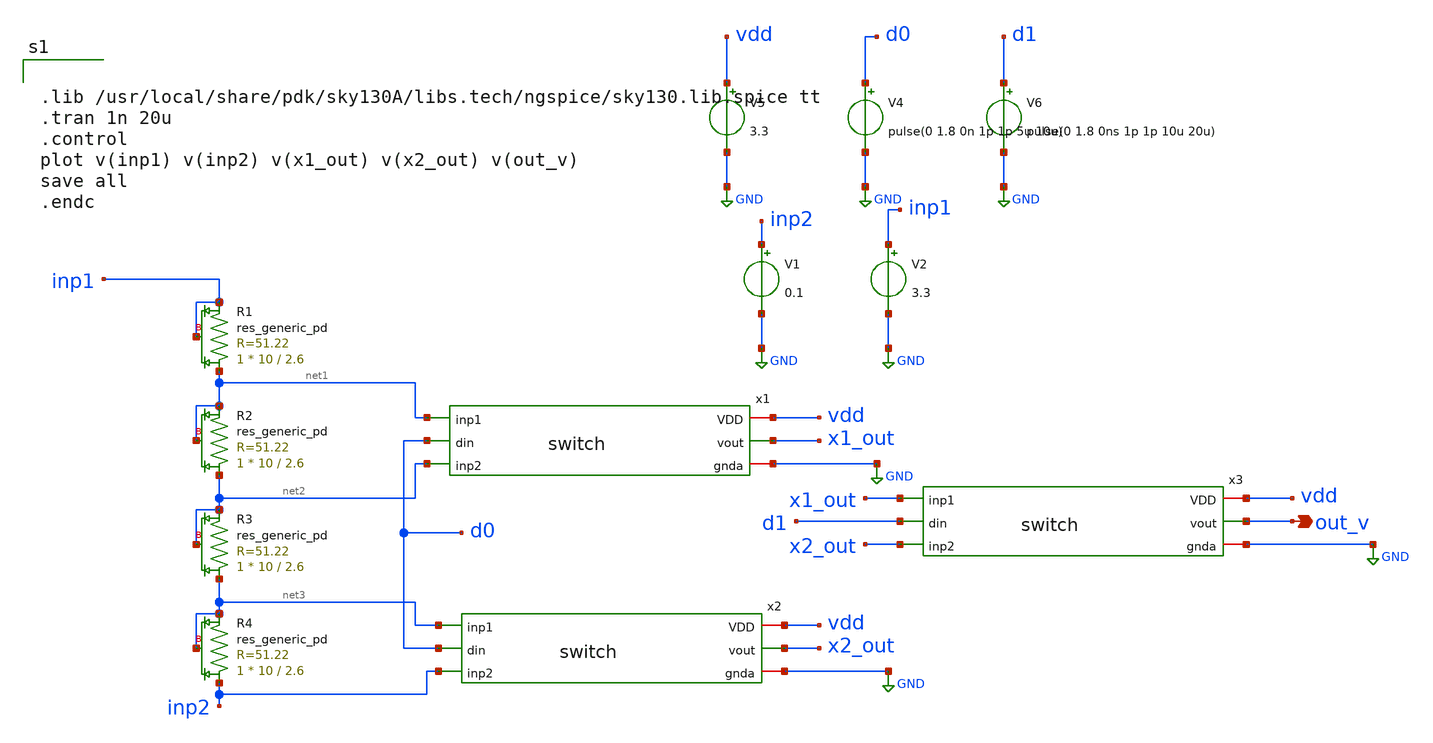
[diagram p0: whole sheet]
** sch_path: week7/pre-layout/two_bit_DAC_tb.sch
**.subckt two_bit_DAC_tb out_v
*.opin out_v
XR1 net1 inp1 inp1 sky130_fd_pr__res_generic_pd W=10 L=2.6 mult=1 m=1
XR2 net2 net1 net1 sky130_fd_pr__res_generic_pd W=10 L=2.6 mult=1 m=1
XR3 net3 net2 net2 sky130_fd_pr__res_generic_pd W=10 L=2.6 mult=1 m=1
XR4 inp2 net3 net3 sky130_fd_pr__res_generic_pd W=10 L=2.6 mult=1 m=1
V1 inp2 GND 0.1
V2 inp1 GND 3.3
V4 d0 GND pulse(0 1.8 0n 1p 1p 5u 10u)
V5 vdd GND 3.3
V6 d1 GND pulse(0 1.8 0ns 1p 1p 10u 20u)
x1 net1 vdd d0 x1_out GND net2 switch
x2 net3 vdd d0 x2_out GND inp2 switch
x3 x1_out vdd d1 out_v GND x2_out switch
**** begin user architecture code


.lib /usr/local/share/pdk/sky130A/libs.tech/ngspice/sky130.lib.spice tt
.tran 1n 20u
.control
plot v(inp1) v(inp2) v(x1_out) v(x2_out) v(out_v)
save all
.endc


**** end user architecture code
**.ends

* expanding   symbol:  switch.sym # of pins=6
** sym_path: week7/pre-layout/switch.sym
** sch_path: week7/pre-layout/switch.sch
.subckt switch inp1 VDD din vout gnda inp2
*.ipin din
*.iopin VDD
*.ipin inp1
*.ipin inp2
*.iopin gnda
*.opin vout
XM1 net1 din gnda gnda sky130_fd_pr__nfet_01v8 L=0.15 W=0.6 nf=1 ad='int((nf+1)/2) * W/nf * 0.29' as='int((nf+2)/2) * W/nf * 0.29'
+ pd='2*int((nf+1)/2) * (W/nf + 0.29)' ps='2*int((nf+2)/2) * (W/nf + 0.29)' nrd='0.29 / W' nrs='0.29 / W'
+ sa=0 sb=0 sd=0 mult=1 m=1
XM2 net1 din VDD VDD sky130_fd_pr__pfet_01v8 L=0.15 W=1.2 nf=1 ad='int((nf+1)/2) * W/nf * 0.29' as='int((nf+2)/2) * W/nf * 0.29'
+ pd='2*int((nf+1)/2) * (W/nf + 0.29)' ps='2*int((nf+2)/2) * (W/nf + 0.29)' nrd='0.29 / W' nrs='0.29 / W'
+ sa=0 sb=0 sd=0 mult=1 m=1
XM3 net2 net1 VDD VDD sky130_fd_pr__pfet_01v8 L=0.15 W=1.2 nf=1 ad='int((nf+1)/2) * W/nf * 0.29' as='int((nf+2)/2) * W/nf * 0.29'
+ pd='2*int((nf+1)/2) * (W/nf + 0.29)' ps='2*int((nf+2)/2) * (W/nf + 0.29)' nrd='0.29 / W' nrs='0.29 / W'
+ sa=0 sb=0 sd=0 mult=1 m=1
XM4 net2 net1 gnda gnda sky130_fd_pr__nfet_01v8 L=0.15 W=0.6 nf=1 ad='int((nf+1)/2) * W/nf * 0.29' as='int((nf+2)/2) * W/nf * 0.29'
+ pd='2*int((nf+1)/2) * (W/nf + 0.29)' ps='2*int((nf+2)/2) * (W/nf + 0.29)' nrd='0.29 / W' nrs='0.29 / W'
+ sa=0 sb=0 sd=0 mult=1 m=1
XM5 inp2 net2 vout VDD sky130_fd_pr__pfet_01v8 L=0.15 W=1.2 nf=1 ad='int((nf+1)/2) * W/nf * 0.29' as='int((nf+2)/2) * W/nf * 0.29'
+ pd='2*int((nf+1)/2) * (W/nf + 0.29)' ps='2*int((nf+2)/2) * (W/nf + 0.29)' nrd='0.29 / W' nrs='0.29 / W'
+ sa=0 sb=0 sd=0 mult=1 m=1
XM6 inp1 net2 vout GND sky130_fd_pr__nfet_01v8 L=0.15 W=0.6 nf=1 ad='int((nf+1)/2) * W/nf * 0.29' as='int((nf+2)/2) * W/nf * 0.29'
+ pd='2*int((nf+1)/2) * (W/nf + 0.29)' ps='2*int((nf+2)/2) * (W/nf + 0.29)' nrd='0.29 / W' nrs='0.29 / W'
+ sa=0 sb=0 sd=0 mult=1 m=1
XM7 vout net1 inp2 GND sky130_fd_pr__nfet_01v8 L=0.15 W=0.6 nf=1 ad='int((nf+1)/2) * W/nf * 0.29' as='int((nf+2)/2) * W/nf * 0.29'
+ pd='2*int((nf+1)/2) * (W/nf + 0.29)' ps='2*int((nf+2)/2) * (W/nf + 0.29)' nrd='0.29 / W' nrs='0.29 / W'
+ sa=0 sb=0 sd=0 mult=1 m=1
XM8 vout net1 inp1 VDD sky130_fd_pr__pfet_01v8 L=0.15 W=1.2 nf=1 ad='int((nf+1)/2) * W/nf * 0.29' as='int((nf+2)/2) * W/nf * 0.29'
+ pd='2*int((nf+1)/2) * (W/nf + 0.29)' ps='2*int((nf+2)/2) * (W/nf + 0.29)' nrd='0.29 / W' nrs='0.29 / W'
+ sa=0 sb=0 sd=0 mult=1 m=1
.ends

.GLOBAL GND
.end
